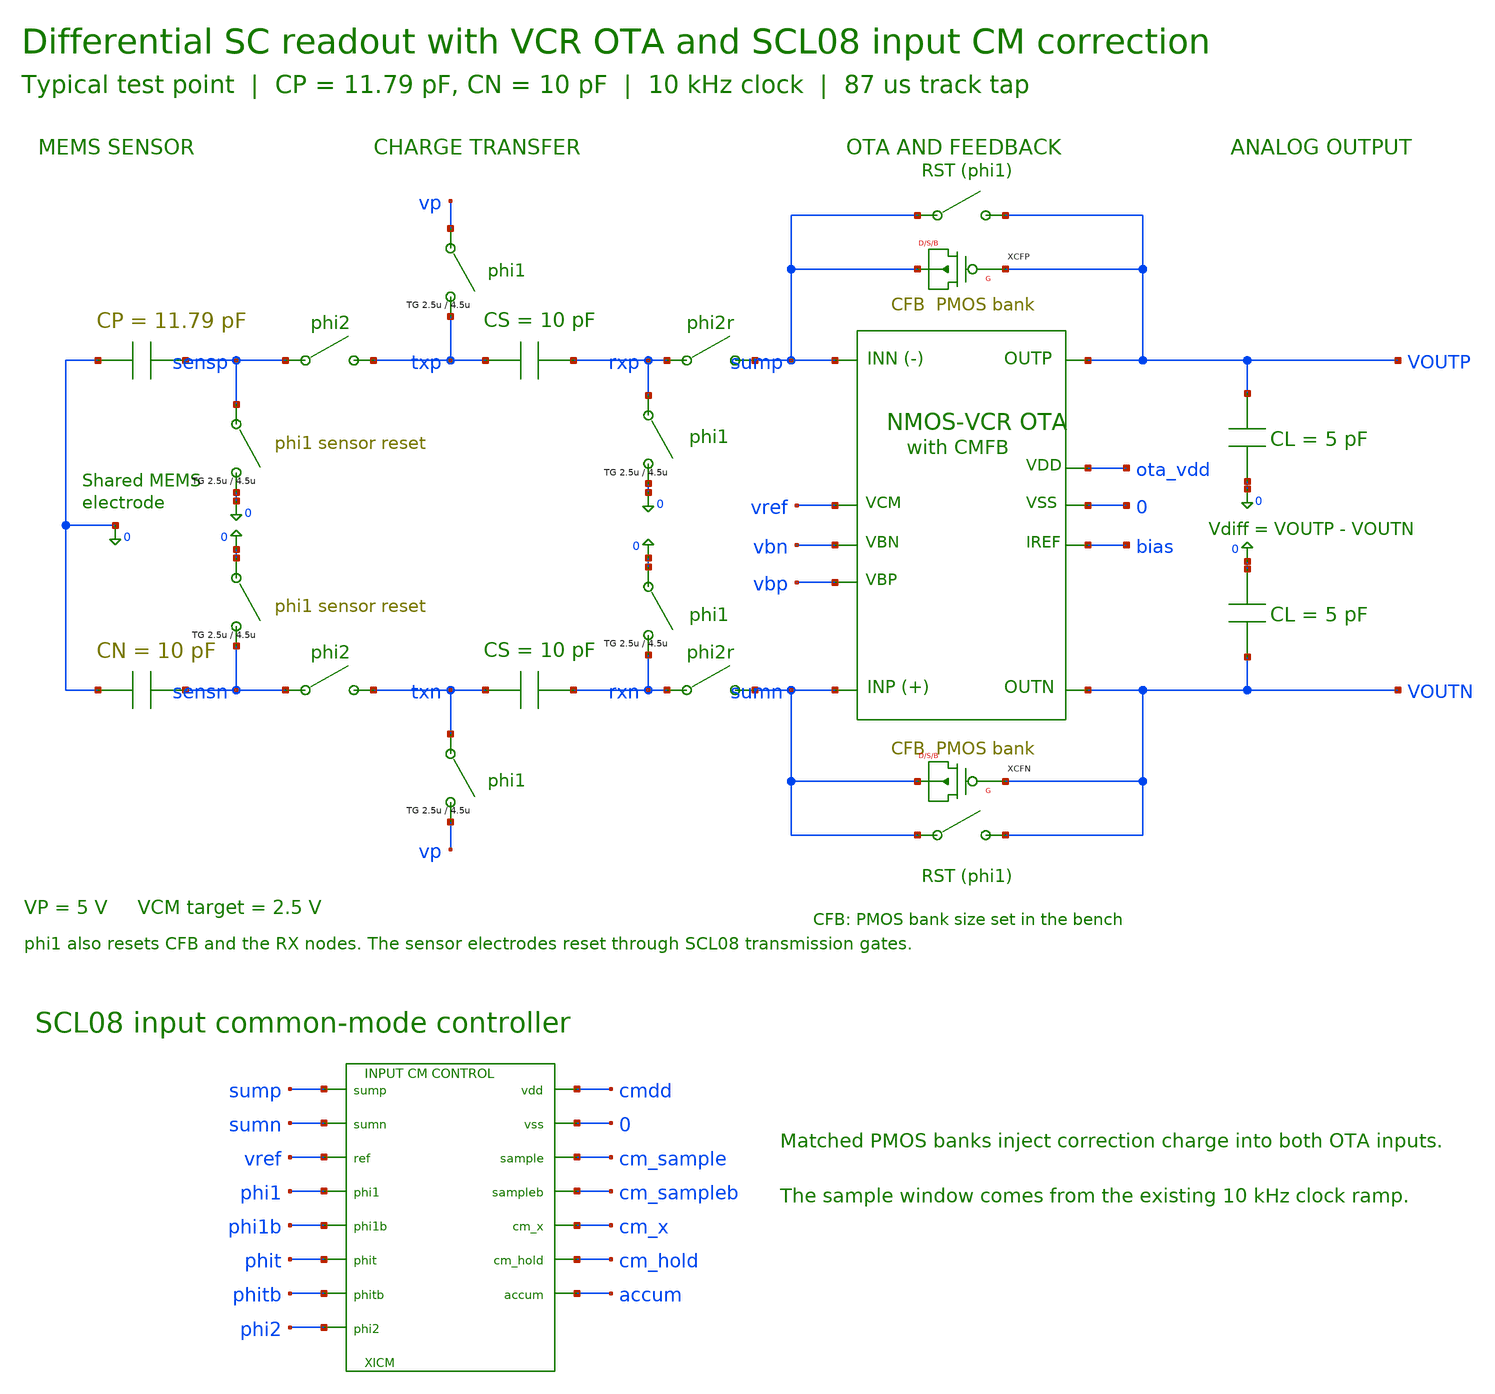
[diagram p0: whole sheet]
** sch_path: Fully_Integrated_Design/transistor_level_icmc/schematic/sc_vcr_input_cm_scl08.sch
**.subckt sc_vcr_input_cm_scl08
XOTA sumn sump outp outn ota_vdd 0 bias vref vbn vbp ota_telescopic_cm2p5
CMEMP 0 sensp 11.79p
XSENSEP sensp txp phi2 phi2b vdd 0 corrected_tg
XSRESETP phi1 0 sensp 0 vdd phi1b Transmission_v1_26
XCHARGEP phi1 0 vp txp vdd phi1b Transmission_v1_26
CSP txp rxp 10p
XRRESETP phi1 0 rxp 0 vdd phi1b Transmission_v1_26
XXFERP rxp sump phit phitb vdd 0 corrected_tg
XCFP sump outp sump sump P W=20u L=202.7u M=5 AD='( 20u ) * 4.5u' AS='( 20u ) * 4.5u' PD='2 * ( 20u ) + 9u'
+ PS='2 * ( 20u ) + 9u'
XFBRESETP sump outp phi1 phi1b vdd 0 corrected_tg
CLP outp 0 5p
CMEMN 0 sensn 10p
XSENSEN sensn txn phi2 phi2b vdd 0 corrected_tg
XSRESETN phi1 0 0 sensn vdd phi1b Transmission_v1_26
XCHARGEN phi1 0 txn vp vdd phi1b Transmission_v1_26
CSN txn rxn 10p
XRRESETN phi1 0 0 rxn vdd phi1b Transmission_v1_26
XXFERN rxn sumn phit phitb vdd 0 corrected_tg
XCFN sumn outn sumn sumn P W=20u L=202.7u M=5 AD='( 20u ) * 4.5u' AS='( 20u ) * 4.5u' PD='2 * ( 20u ) + 9u'
+ PS='2 * ( 20u ) + 9u'
XFBRESETN sumn outn phi1 phi1b vdd 0 corrected_tg
CLN 0 outn 5p
XICM sump sumn vref phi1 phi1b phit phitb phi2 cmdd 0 cm_sample cm_sampleb cm_x cm_hold accum
+ icm_cell08
**** begin user architecture code
.include bench_support.spice
**** end user architecture code
**.ends

* expanding   symbol:  icm_cell08.sym # of pins=15
** sym_path: ICMC/schematic/icm_cell08.sym
** sch_path: ICMC/schematic/icm_cell08.sch
.subckt icm_cell08 sump sumn ref phi1 phi1b phit phitb phi2 vdd vss sample sampleb cm_x cm_hold
+ accum
*.iopin sump
*.iopin sumn
*.iopin ref
*.iopin phi1
*.iopin phi1b
*.iopin phit
*.iopin phitb
*.iopin phi2
*.iopin vdd
*.iopin vss
*.iopin sample
*.iopin sampleb
*.iopin cm_x
*.iopin cm_hold
*.iopin accum
XRBIAS vdd nb RPP W=2.4u L=20000u
MBIAS nb nb vss vss N w=20u l=2.4u m=1
XEP sump ref current sample vdd vss nb icm_error08
XEN sumn ref current sample vdd vss nb icm_error08
XUP current accum sample sampleb vdd vss icm_tg08
XPRE drive current sampleb sample vdd vss icm_tg08
MCINT vdd accum vdd vdd P w=100u l=20u m=9
MCH vdd cm_hold vdd vdd P w=100u l=20u m=1
MLOW ref ref accum vss N w=2.5u l=4u m=1
MHIGH accum ref ref vdd P w=2.5u l=4u m=1
XLATCH accum cm_hold phi1 phi1b vdd vss icm_tg08
XBUF cm_hold drive vdd vss nb icm_buffer08
XTXB phi2 tx_b vdd vss inv08 w=3u
XTXA tx_b tx_a vdd vss inv08 w=12u
XRXHI drive edge_r phit phitb vdd vss icm_drive_tg08
XRXLO vss edge_r phitb phit vdd vss icm_drive_tg08
XTXHI drive edge_t tx_a tx_b vdd vss icm_drive_tg08
XTXLO vss edge_t tx_b tx_a vdd vss icm_drive_tg08
XR1 edge_r cm_x RPP W=2.4u L=350u
XR2 edge_t cm_x RPP W=2.4u L=744u
MCORRP sump cm_x sump sump P w=20u l=10u ad=90p as=90p pd=49u ps=49u m=40
MCORRN sumn cm_x sumn sumn P w=20u l=10u ad=90p as=90p pd=49u ps=49u m=40
.ends


* expanding   symbol:  icm_error08.sym # of pins=7
** sym_path: ICMC/schematic/icm_error08.sym
** sch_path: ICMC/schematic/icm_error08.sch
.subckt icm_error08 inp ref drive sample vdd vss nb
*.iopin inp
*.iopin ref
*.iopin drive
*.iopin sample
*.iopin vdd
*.iopin vss
*.iopin nb
MREF mirror ref tail vss N w=12u l=2.4u m=1
MSIG drive inp tail vss N w=12u l=2.4u m=1
MEN tail sample sink vss N w=8u l=.8u m=1
MT sink nb vss vss N w=6u l=8u m=1
MP0 mirror mirror vdd vdd P w=12u l=4u m=1
MP1 drive mirror vdd vdd P w=12u l=4u m=1
.ends


* expanding   symbol:  icm_tg08.sym # of pins=6
** sym_path: ICMC/schematic/icm_tg08.sym
** sch_path: ICMC/schematic/icm_tg08.sch
.subckt icm_tg08 a b en enb vdd vss
*.iopin a
*.iopin b
*.iopin en
*.iopin enb
*.iopin vdd
*.iopin vss
MN a en b vss N w=4u l=.8u ad=18p as=18p pd=17u ps=17u m=1
MP a enb b vdd P w=8u l=.8u ad=36p as=36p pd=25u ps=25u m=1
.ends


* expanding   symbol:  icm_buffer08.sym # of pins=5
** sym_path: ICMC/schematic/icm_buffer08.sym
** sch_path: ICMC/schematic/icm_buffer08.sch
.subckt icm_buffer08 hold out vdd vss nb
*.iopin hold
*.iopin out
*.iopin vdd
*.iopin vss
*.iopin nb
MIN nleft out tail vss N w=20u l=2.4u m=1
MREF gain hold tail vss N w=20u l=2.4u m=1
MTAIL tail nb vss vss N w=8u l=4.8u m=1
MP0 nleft nleft vdd vdd P w=10u l=3.2u m=1
MP1 gain nleft vdd vdd P w=10u l=3.2u m=1
MP2 out gain vdd vdd P w=100u l=1.6u m=1
MN2 out nb vss vss N w=12u l=4.8u m=1
MCOMP out gain out out P w=30u l=12u m=2
.ends


* expanding   symbol:  icm_drive_tg08.sym # of pins=6
** sym_path: ICMC/schematic/icm_drive_tg08.sym
** sch_path: ICMC/schematic/icm_drive_tg08.sch
.subckt icm_drive_tg08 a b en enb vdd vss
*.iopin a
*.iopin b
*.iopin en
*.iopin enb
*.iopin vdd
*.iopin vss
MN a en b vss N w=12u l=.8u ad=54p as=54p pd=33u ps=33u m=1
MP a enb b vdd P w=24u l=.8u ad=108p as=108p pd=57u ps=57u m=1
.ends

.end
